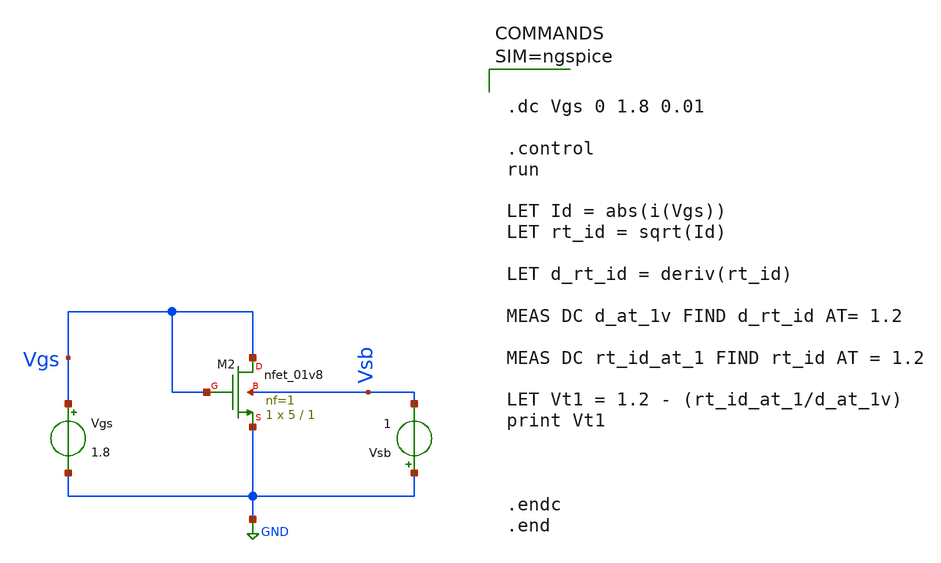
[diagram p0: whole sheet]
** sch_path: sch/lev0_1-val.sch
**.subckt lev0_1-val
XM2 Vgs Vgs GND Vsb sky130_fd_pr__nfet_01v8 L=1 W=5 nf=1 ad='int((1 + 1)/2) * 5 / 1 * 0.29' as='int((1 + 2)/2) * 5 / 1 * 0.29'
+ pd='2*int((1 + 1)/2) * (5 / 1 + 0.29)' ps='2*int((1 + 2)/2) * (5 / 1 + 0.29)' nrd='0.29 / 5 ' nrs='0.29 / 5 '
+ sa=0 sb=0 sd=0 mult=1 m=1
Vgs Vgs GND 1.8
Vsb GND Vsb 1
**** begin user architecture code

** opencircuitdesign pdks install
.lib $::SKYWATER_MODELS/sky130.lib.spice tt




.dc Vgs 0 1.8 0.01

.control
run

LET Id = abs(i(Vgs))
LET rt_id = sqrt(Id)

LET d_rt_id = deriv(rt_id)

MEAS DC d_at_1v FIND d_rt_id AT= 1.2

MEAS DC rt_id_at_1 FIND rt_id AT = 1.2

LET Vt1 = 1.2 - (rt_id_at_1/d_at_1v)
print Vt1



.endc
.end



**** end user architecture code
**.ends
.GLOBAL GND
.end
